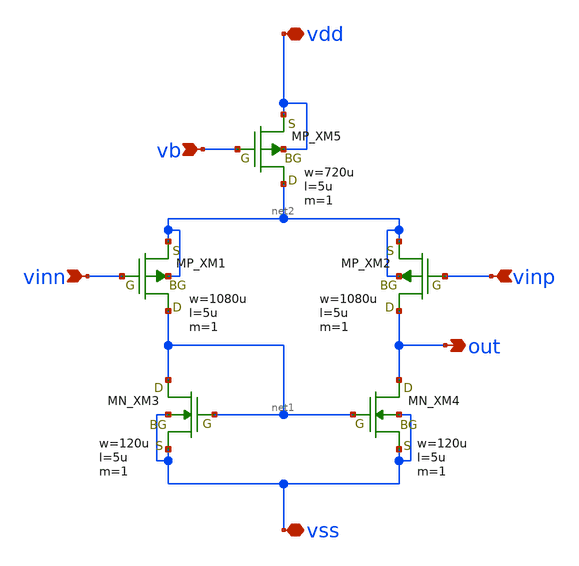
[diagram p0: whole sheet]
** sch_path: member_project/OPAMP/kano/sch_tb/diff.sch
**.subckt diff vinn vinp vb out vdd vss
*.ipin vinn
*.ipin vinp
*.ipin vb
*.opin out
*.iopin vdd
*.iopin vss
XM5 net2 vb vdd vdd PMOS w=720u l=5u as=0 ad=0 ps=0 pd=0 nrd=0 nrs=0 m=1
XM1 net1 vinn net2 net2 PMOS w=1080u l=5u as=0 ad=0 ps=0 pd=0 nrd=0 nrs=0 m=1
XM2 out vinp net2 net2 PMOS w=1080u l=5u as=0 ad=0 ps=0 pd=0 nrd=0 nrs=0 m=1
XM3 net1 net1 vss vss NMOS w=120u l=5u as=0 ad=0 ps=0 pd=0 nrd=0 nrs=0 m=1
XM4 out net1 vss vss NMOS w=120u l=5u as=0 ad=0 ps=0 pd=0 nrd=0 nrs=0 m=1
**.ends
.end
